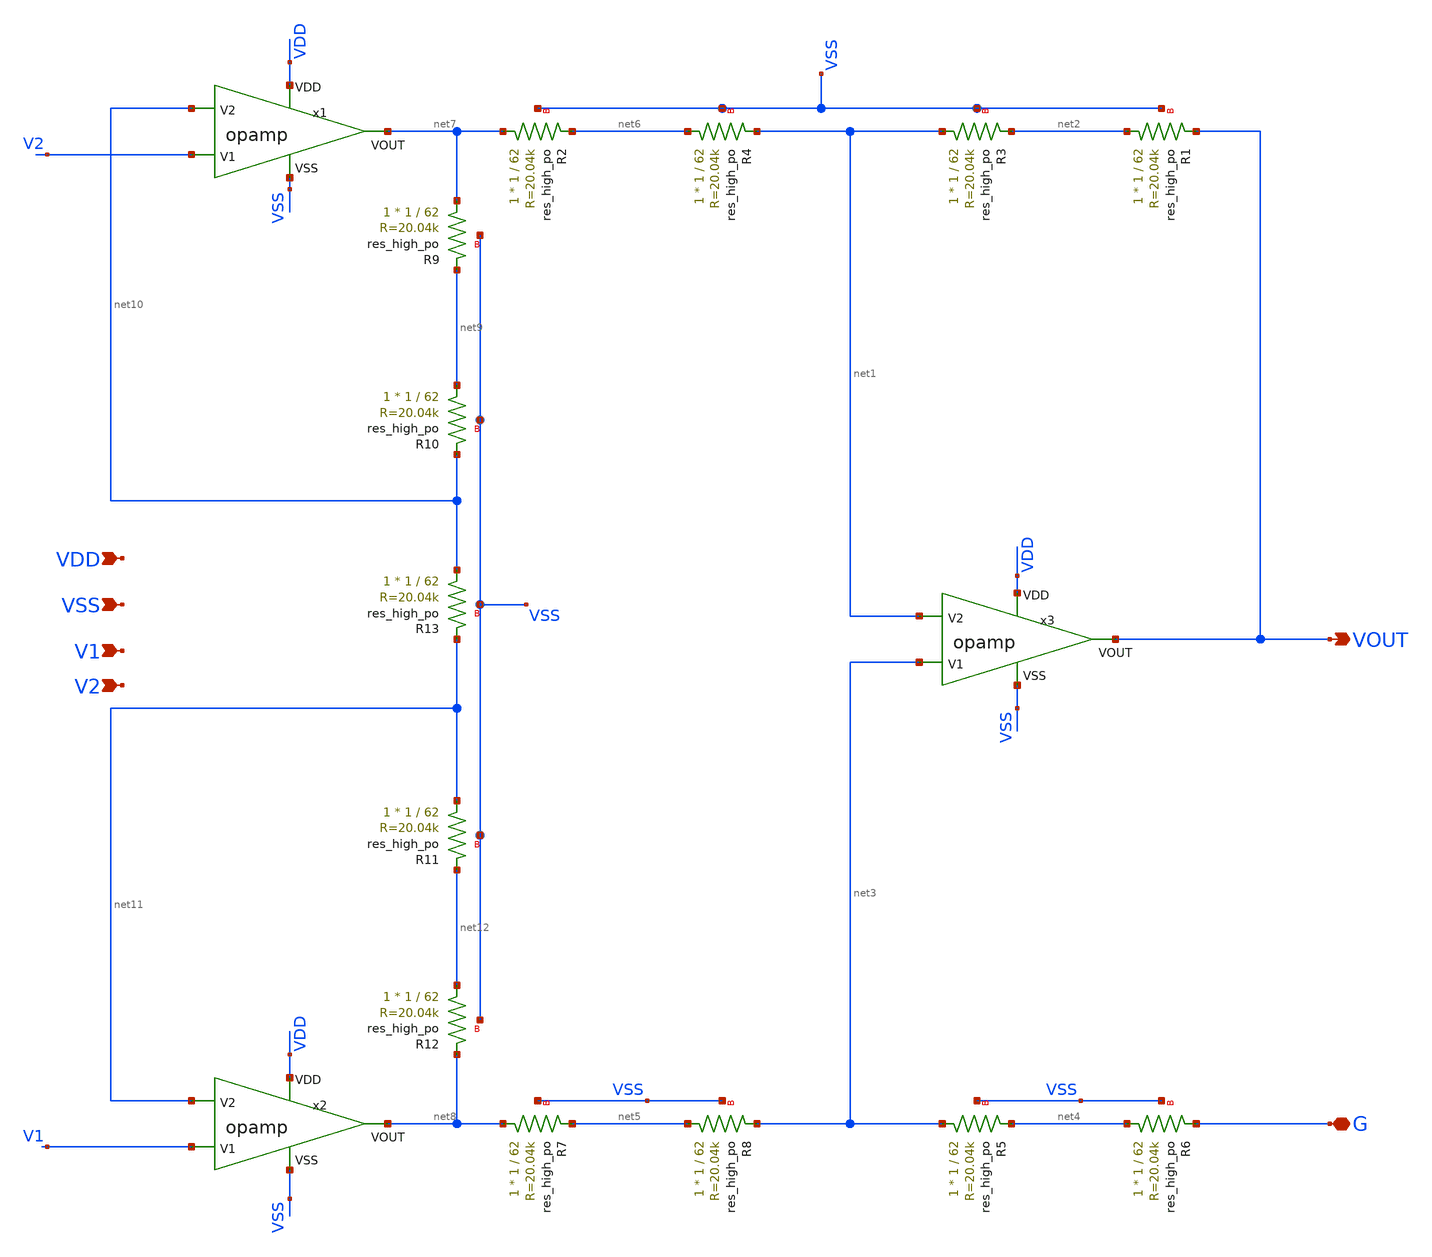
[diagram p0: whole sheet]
** sch_path: final.sch
**.subckt final VOUT G VDD VSS V1 V2
*.opin VOUT
*.iopin G
*.ipin VDD
*.ipin VSS
*.ipin V1
*.ipin V2
XR3 net1 net2 VSS sky130_fd_pr__res_high_po W=1 L=62 mult=1 m=1
XR1 net2 VOUT VSS sky130_fd_pr__res_high_po W=1 L=62 mult=1 m=1
XR2 net7 net6 VSS sky130_fd_pr__res_high_po W=1 L=62 mult=1 m=1
XR4 net6 net1 VSS sky130_fd_pr__res_high_po W=1 L=62 mult=1 m=1
XR5 net3 net4 VSS sky130_fd_pr__res_high_po W=1 L=62 mult=1 m=1
XR6 net4 G VSS sky130_fd_pr__res_high_po W=1 L=62 mult=1 m=1
XR7 net8 net5 VSS sky130_fd_pr__res_high_po W=1 L=62 mult=1 m=1
XR8 net5 net3 VSS sky130_fd_pr__res_high_po W=1 L=62 mult=1 m=1
XR9 net7 net9 VSS sky130_fd_pr__res_high_po W=1 L=62 mult=1 m=1
XR10 net9 net10 VSS sky130_fd_pr__res_high_po W=1 L=62 mult=1 m=1
XR11 net11 net12 VSS sky130_fd_pr__res_high_po W=1 L=62 mult=1 m=1
XR12 net12 net8 VSS sky130_fd_pr__res_high_po W=1 L=62 mult=1 m=1
XR13 net10 net11 VSS sky130_fd_pr__res_high_po W=1 L=62 mult=1 m=1
x1 VDD VSS V2 net10 net7 opamp
x2 VDD VSS V1 net11 net8 opamp
x3 VDD VSS net3 net1 VOUT opamp
**.ends

* expanding   symbol:  /foss/designs/chipalooza2024/sky130_hcmus_ip__instramp/opamp.sym # of pins=5
** sym_path: xschem/opamp.sym
** sch_path: xschem/opamp.sch
.subckt opamp VDD VSS V1 V2 VOUT
*.ipin VSS
*.ipin VDD
*.ipin V2
*.ipin V1
*.opin VOUT
XM2 net4 V2 net1 VSS sky130_fd_pr__nfet_g5v0d10v5 L=1 W=18 nf=1 ad='int((nf+1)/2) * W/nf * 0.29' as='int((nf+2)/2) * W/nf * 0.29'
+ pd='2*int((nf+1)/2) * (W/nf + 0.29)' ps='2*int((nf+2)/2) * (W/nf + 0.29)' nrd='0.29 / W' nrs='0.29 / W'
+ sa=0 sb=0 sd=0 mult=1 m=1
XM1 net5 net4 VDD VDD sky130_fd_pr__pfet_g5v0d10v5 L=1 W=30 nf=1 ad='int((nf+1)/2) * W/nf * 0.29' as='int((nf+2)/2) * W/nf * 0.29'
+ pd='2*int((nf+1)/2) * (W/nf + 0.29)' ps='2*int((nf+2)/2) * (W/nf + 0.29)' nrd='0.29 / W' nrs='0.29 / W'
+ sa=0 sb=0 sd=0 mult=1 m=1
XM4 net5 V1 net1 VSS sky130_fd_pr__nfet_g5v0d10v5 L=1 W=18 nf=1 ad='int((nf+1)/2) * W/nf * 0.29' as='int((nf+2)/2) * W/nf * 0.29'
+ pd='2*int((nf+1)/2) * (W/nf + 0.29)' ps='2*int((nf+2)/2) * (W/nf + 0.29)' nrd='0.29 / W' nrs='0.29 / W'
+ sa=0 sb=0 sd=0 mult=1 m=1
XM5 net1 net6 VSS VSS sky130_fd_pr__nfet_g5v0d10v5 L=1 W=15.171 nf=1 ad='int((nf+1)/2) * W/nf * 0.29'
+ as='int((nf+2)/2) * W/nf * 0.29' pd='2*int((nf+1)/2) * (W/nf + 0.29)' ps='2*int((nf+2)/2) * (W/nf + 0.29)'
+ nrd='0.29 / W' nrs='0.29 / W' sa=0 sb=0 sd=0 mult=1 m=1
XM6 VOUT net6 VSS VSS sky130_fd_pr__nfet_g5v0d10v5 L=1 W=19 nf=1 ad='int((nf+1)/2) * W/nf * 0.29' as='int((nf+2)/2) * W/nf * 0.29'
+ pd='2*int((nf+1)/2) * (W/nf + 0.29)' ps='2*int((nf+2)/2) * (W/nf + 0.29)' nrd='0.29 / W' nrs='0.29 / W'
+ sa=0 sb=0 sd=0 mult=1 m=1
XM7 net6 net6 VSS VSS sky130_fd_pr__nfet_g5v0d10v5 L=1 W=20 nf=1 ad='int((nf+1)/2) * W/nf * 0.29' as='int((nf+2)/2) * W/nf * 0.29'
+ pd='2*int((nf+1)/2) * (W/nf + 0.29)' ps='2*int((nf+2)/2) * (W/nf + 0.29)' nrd='0.29 / W' nrs='0.29 / W'
+ sa=0 sb=0 sd=0 mult=1 m=1
XM3 net4 net4 VDD VDD sky130_fd_pr__pfet_g5v0d10v5 L=1 W=30 nf=1 ad='int((nf+1)/2) * W/nf * 0.29' as='int((nf+2)/2) * W/nf * 0.29'
+ pd='2*int((nf+1)/2) * (W/nf + 0.29)' ps='2*int((nf+2)/2) * (W/nf + 0.29)' nrd='0.29 / W' nrs='0.29 / W'
+ sa=0 sb=0 sd=0 mult=1 m=1
XM8 VOUT net5 VDD VDD sky130_fd_pr__pfet_g5v0d10v5 L=1 W=38 nf=1 ad='int((nf+1)/2) * W/nf * 0.29' as='int((nf+2)/2) * W/nf * 0.29'
+ pd='2*int((nf+1)/2) * (W/nf + 0.29)' ps='2*int((nf+2)/2) * (W/nf + 0.29)' nrd='0.29 / W' nrs='0.29 / W'
+ sa=0 sb=0 sd=0 mult=2 m=2
XC1 net7 net5 sky130_fd_pr__cap_mim_m3_1 W=5.5 L=10 MF=10 m=10
V_ibias net8 net6 0
.save i(v_ibias)
XR5 net2 VDD VSS sky130_fd_pr__res_high_po_0p69 L=18.58 mult=1 m=1
XR1 net3 net2 VSS sky130_fd_pr__res_high_po_0p69 L=18.58 mult=1 m=1
XR2 net8 net3 VSS sky130_fd_pr__res_high_po_0p69 L=18.58 mult=1 m=1
XR3 net7 VOUT VSS sky130_fd_pr__res_high_po_0p69 L=2.41 mult=1 m=1
.ends

.end
